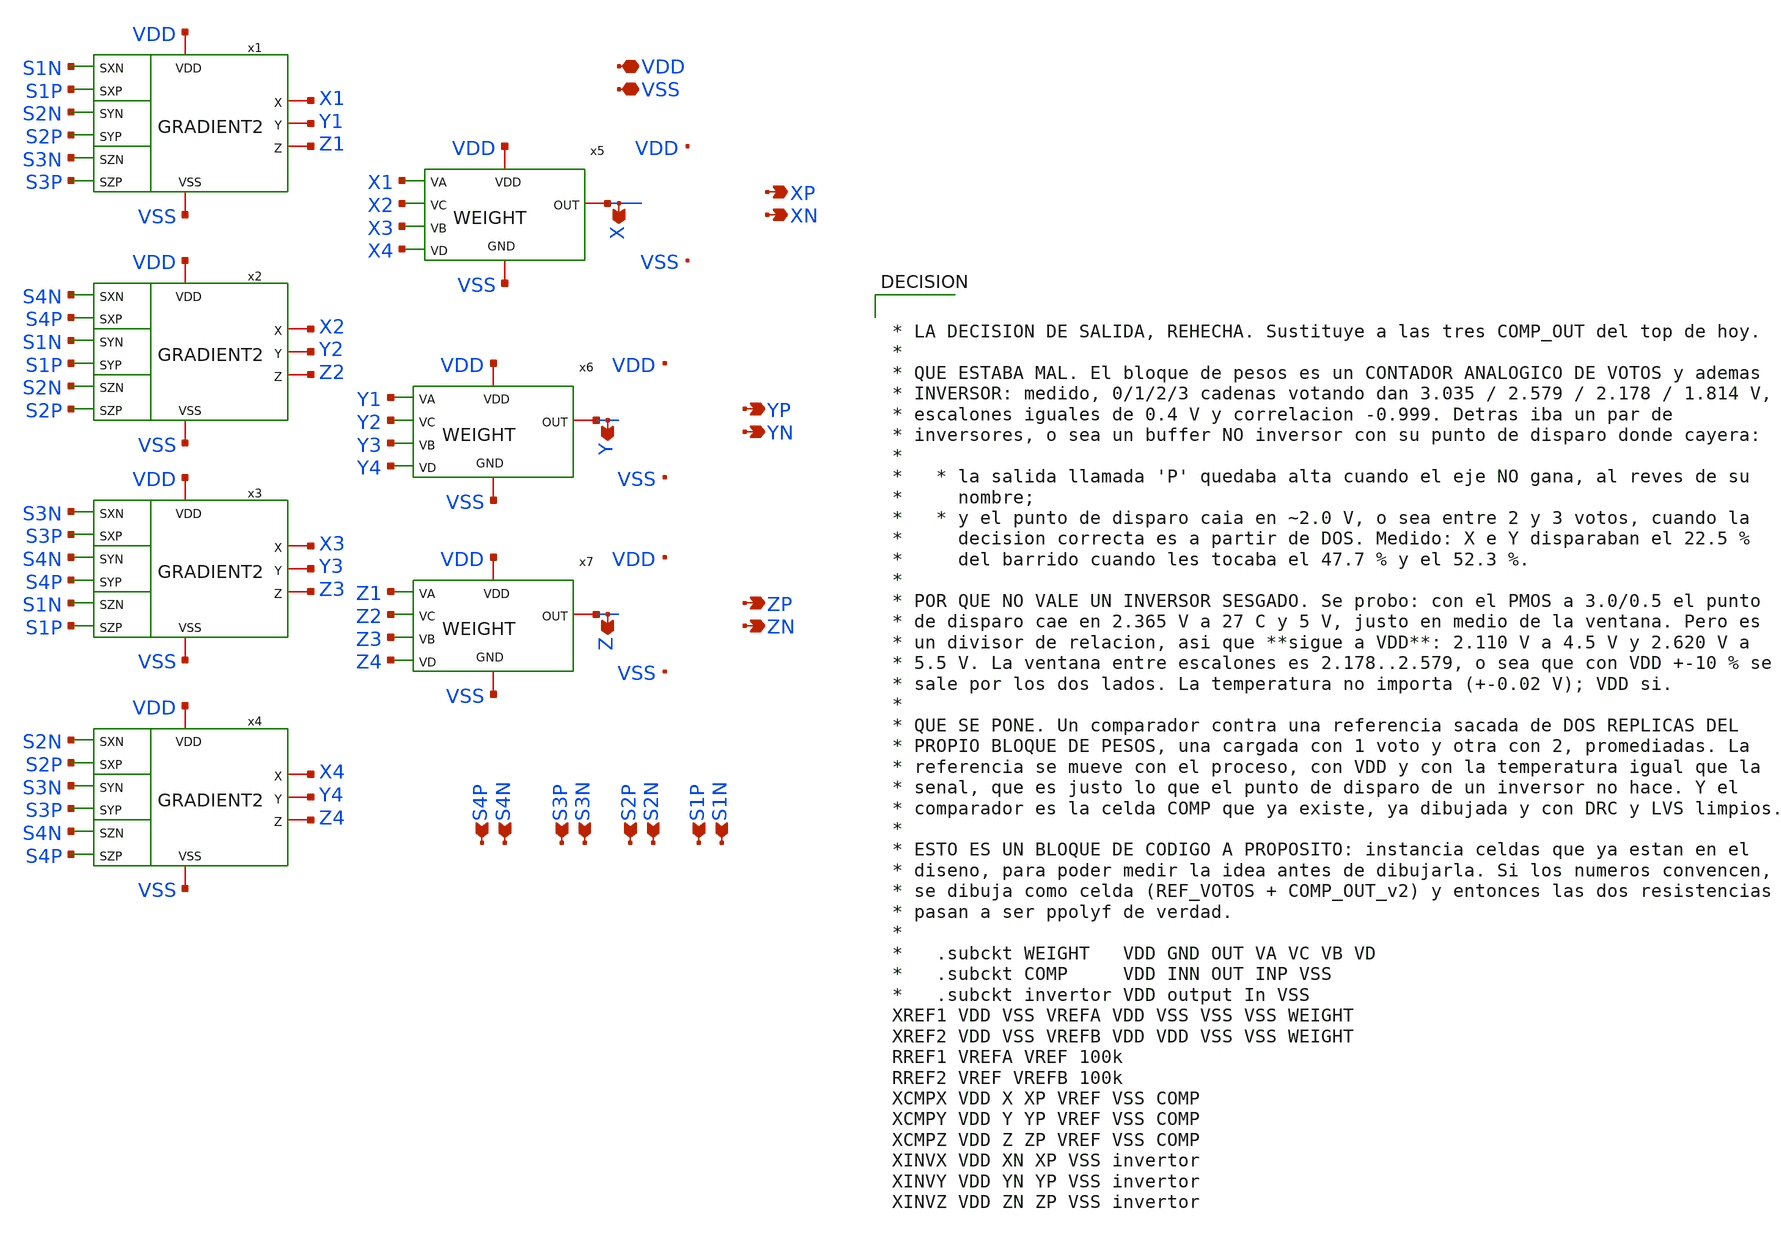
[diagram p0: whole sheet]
** sch_path: FINAL/XSCHEM_v2/GRADIENT_NAV2_V2.sch
**.subckt GRADIENT_NAV2_V2 S1N VDD XN VSS S1P S2N S2P S3N S3P S4N S4P XP YN YP ZN ZP X Y Z
*.ipin S1N
*.iopin VDD
*.opin XN
*.iopin VSS
*.ipin S1P
*.ipin S2N
*.ipin S2P
*.ipin S3N
*.ipin S3P
*.ipin S4N
*.ipin S4P
*.opin XP
*.opin YN
*.opin YP
*.opin ZN
*.opin ZP
*.opin X
*.opin Y
*.opin Z
x5 VDD VSS X X1 X2 X3 X4 WEIGHT
x6 VDD VSS Y Y1 Y2 Y3 Y4 WEIGHT
x7 VDD VSS Z Z1 Z2 Z3 Z4 WEIGHT
x1 S1N S1P VDD X1 S2N Y1 Z1 S2P VSS S3N S3P GRADIENT2
x2 S4N S4P VDD X2 S1N Y2 Z2 S1P VSS S2N S2P GRADIENT2
x3 S3N S3P VDD X3 S4N Y3 Z3 S4P VSS S1N S1P GRADIENT2
x4 S2N S2P VDD X4 S3N Y4 Z4 S3P VSS S4N S4P GRADIENT2
**** begin user architecture code


* Condensadores de desacople: NMOS y PMOS en inversion metidos en
* los huecos entre macros. LO ESCRIBE scripts/decap_fill.py -- no
* se edita a mano: tiene que ser exactamente lo que hay en el GDS.
XMdecn0 VSS VDD VSS VSS nfet_06v0 L=2.0u W=1.5u nf=1 m=1
XMdecn1 VSS VDD VSS VSS nfet_06v0 L=2.0u W=1.5u nf=1 m=1
XMdecn2 VSS VDD VSS VSS nfet_06v0 L=2.0u W=1.5u nf=1 m=1
XMdecn3 VSS VDD VSS VSS nfet_06v0 L=2.0u W=1.5u nf=1 m=1
XMdecn4 VSS VDD VSS VSS nfet_06v0 L=2.0u W=1.5u nf=1 m=1
XMdecn5 VSS VDD VSS VSS nfet_06v0 L=2.0u W=1.5u nf=1 m=1
XMdecn6 VSS VDD VSS VSS nfet_06v0 L=2.0u W=1.5u nf=1 m=1
XMdecn7 VSS VDD VSS VSS nfet_06v0 L=2.0u W=1.5u nf=1 m=1
XMdecn8 VSS VDD VSS VSS nfet_06v0 L=2.0u W=1.5u nf=1 m=1
XMdecn9 VSS VDD VSS VSS nfet_06v0 L=2.0u W=1.5u nf=1 m=1
XMdecn10 VSS VDD VSS VSS nfet_06v0 L=2.0u W=1.5u nf=1 m=1
XMdecn11 VSS VDD VSS VSS nfet_06v0 L=2.0u W=1.5u nf=1 m=1
XMdecn12 VSS VDD VSS VSS nfet_06v0 L=2.0u W=1.5u nf=1 m=1
XMdecn13 VSS VDD VSS VSS nfet_06v0 L=2.0u W=1.5u nf=1 m=1
XMdecn14 VSS VDD VSS VSS nfet_06v0 L=2.0u W=1.5u nf=1 m=1
XMdecn15 VSS VDD VSS VSS nfet_06v0 L=2.0u W=1.5u nf=1 m=1
XMdecn16 VSS VDD VSS VSS nfet_06v0 L=2.0u W=1.5u nf=1 m=1
XMdecn17 VSS VDD VSS VSS nfet_06v0 L=2.0u W=1.5u nf=1 m=1
XMdecn18 VSS VDD VSS VSS nfet_06v0 L=2.0u W=1.5u nf=1 m=1
XMdecn19 VSS VDD VSS VSS nfet_06v0 L=2.0u W=1.5u nf=1 m=1
XMdecn20 VSS VDD VSS VSS nfet_06v0 L=2.0u W=1.5u nf=1 m=1
XMdecn21 VSS VDD VSS VSS nfet_06v0 L=2.0u W=1.5u nf=1 m=1
XMdecn22 VSS VDD VSS VSS nfet_06v0 L=2.0u W=1.5u nf=1 m=1
XMdecn23 VSS VDD VSS VSS nfet_06v0 L=2.0u W=1.5u nf=1 m=1
XMdecn24 VSS VDD VSS VSS nfet_06v0 L=2.0u W=1.5u nf=1 m=1
XMdecn25 VSS VDD VSS VSS nfet_06v0 L=2.0u W=1.5u nf=1 m=1
XMdecn26 VSS VDD VSS VSS nfet_06v0 L=2.0u W=1.5u nf=1 m=1
XMdecn27 VSS VDD VSS VSS nfet_06v0 L=2.0u W=1.5u nf=1 m=1
XMdecn28 VSS VDD VSS VSS nfet_06v0 L=2.0u W=1.5u nf=1 m=1
XMdecn29 VSS VDD VSS VSS nfet_06v0 L=2.0u W=1.5u nf=1 m=1
XMdecn30 VSS VDD VSS VSS nfet_06v0 L=2.0u W=1.5u nf=1 m=1
XMdecn31 VSS VDD VSS VSS nfet_06v0 L=2.0u W=1.5u nf=1 m=1
XMdecn32 VSS VDD VSS VSS nfet_06v0 L=2.0u W=1.5u nf=1 m=1
XMdecn33 VSS VDD VSS VSS nfet_06v0 L=2.0u W=1.5u nf=1 m=1
XMdecn34 VSS VDD VSS VSS nfet_06v0 L=2.0u W=1.5u nf=1 m=1
XMdecn35 VSS VDD VSS VSS nfet_06v0 L=2.0u W=1.5u nf=1 m=1
XMdecn36 VSS VDD VSS VSS nfet_06v0 L=2.0u W=1.5u nf=1 m=1
XMdecn37 VSS VDD VSS VSS nfet_06v0 L=2.0u W=1.5u nf=1 m=1
XMdecn38 VSS VDD VSS VSS nfet_06v0 L=2.0u W=1.5u nf=1 m=1
XMdecn39 VSS VDD VSS VSS nfet_06v0 L=2.0u W=1.5u nf=1 m=1
XMdecn40 VSS VDD VSS VSS nfet_06v0 L=2.0u W=1.5u nf=1 m=1
XMdecn41 VSS VDD VSS VSS nfet_06v0 L=2.0u W=1.5u nf=1 m=1
XMdecn42 VSS VDD VSS VSS nfet_06v0 L=2.0u W=1.5u nf=1 m=1
XMdecn43 VSS VDD VSS VSS nfet_06v0 L=2.0u W=1.5u nf=1 m=1
XMdecn44 VSS VDD VSS VSS nfet_06v0 L=2.0u W=1.5u nf=1 m=1
XMdecn45 VSS VDD VSS VSS nfet_06v0 L=2.0u W=1.5u nf=1 m=1
XMdecn46 VSS VDD VSS VSS nfet_06v0 L=2.0u W=1.5u nf=1 m=1
XMdecn47 VSS VDD VSS VSS nfet_06v0 L=2.0u W=1.5u nf=1 m=1
XMdecn48 VSS VDD VSS VSS nfet_06v0 L=2.0u W=1.5u nf=1 m=1
XMdecn49 VSS VDD VSS VSS nfet_06v0 L=2.0u W=1.5u nf=1 m=1
XMdecn50 VSS VDD VSS VSS nfet_06v0 L=2.0u W=1.5u nf=1 m=1
XMdecn51 VSS VDD VSS VSS nfet_06v0 L=2.0u W=1.5u nf=1 m=1
XMdecn52 VSS VDD VSS VSS nfet_06v0 L=2.0u W=1.5u nf=1 m=1
XMdecp53 VDD VSS VDD VDD pfet_06v0 L=2.0u W=1.5u nf=1 m=1
XMdecp54 VDD VSS VDD VDD pfet_06v0 L=2.0u W=1.5u nf=1 m=1
XMdecp55 VDD VSS VDD VDD pfet_06v0 L=2.0u W=1.5u nf=1 m=1
XMdecp56 VDD VSS VDD VDD pfet_06v0 L=2.0u W=1.5u nf=1 m=1
XMdecp57 VDD VSS VDD VDD pfet_06v0 L=2.0u W=1.5u nf=1 m=1
XMdecp58 VDD VSS VDD VDD pfet_06v0 L=2.0u W=1.5u nf=1 m=1
XMdecp59 VDD VSS VDD VDD pfet_06v0 L=2.0u W=1.5u nf=1 m=1
XMdecp60 VDD VSS VDD VDD pfet_06v0 L=2.0u W=1.5u nf=1 m=1
XMdecp61 VDD VSS VDD VDD pfet_06v0 L=2.0u W=1.5u nf=1 m=1
XMdecp62 VDD VSS VDD VDD pfet_06v0 L=2.0u W=1.5u nf=1 m=1
XMdecp63 VDD VSS VDD VDD pfet_06v0 L=2.0u W=1.5u nf=1 m=1
XMdecp64 VDD VSS VDD VDD pfet_06v0 L=2.0u W=1.5u nf=1 m=1
XMdecp65 VDD VSS VDD VDD pfet_06v0 L=2.0u W=1.5u nf=1 m=1
XMdecp66 VDD VSS VDD VDD pfet_06v0 L=2.0u W=1.5u nf=1 m=1
XMdecp67 VDD VSS VDD VDD pfet_06v0 L=2.0u W=1.5u nf=1 m=1
XMdecp68 VDD VSS VDD VDD pfet_06v0 L=2.0u W=1.5u nf=1 m=1
XMdecp69 VDD VSS VDD VDD pfet_06v0 L=2.0u W=1.5u nf=1 m=1
XMdecp70 VDD VSS VDD VDD pfet_06v0 L=2.0u W=1.5u nf=1 m=1
XMdecp71 VDD VSS VDD VDD pfet_06v0 L=2.0u W=1.5u nf=1 m=1
XMdecp72 VDD VSS VDD VDD pfet_06v0 L=2.0u W=1.5u nf=1 m=1
XMdecp73 VDD VSS VDD VDD pfet_06v0 L=2.0u W=1.5u nf=1 m=1
XMdecp74 VDD VSS VDD VDD pfet_06v0 L=2.0u W=1.5u nf=1 m=1
XMdecp75 VDD VSS VDD VDD pfet_06v0 L=2.0u W=1.5u nf=1 m=1
XMdecp76 VDD VSS VDD VDD pfet_06v0 L=2.0u W=1.5u nf=1 m=1
XMdecp77 VDD VSS VDD VDD pfet_06v0 L=2.0u W=1.5u nf=1 m=1
XMdecp78 VDD VSS VDD VDD pfet_06v0 L=2.0u W=1.5u nf=1 m=1
XMdecp79 VDD VSS VDD VDD pfet_06v0 L=2.0u W=1.5u nf=1 m=1
XMdecp80 VDD VSS VDD VDD pfet_06v0 L=2.0u W=1.5u nf=1 m=1
XMdecp81 VDD VSS VDD VDD pfet_06v0 L=2.0u W=1.5u nf=1 m=1
XMdecp82 VDD VSS VDD VDD pfet_06v0 L=2.0u W=1.5u nf=1 m=1
XMdecp83 VDD VSS VDD VDD pfet_06v0 L=2.0u W=1.5u nf=1 m=1
XMdecp84 VDD VSS VDD VDD pfet_06v0 L=2.0u W=1.5u nf=1 m=1
XMdecp85 VDD VSS VDD VDD pfet_06v0 L=2.0u W=1.5u nf=1 m=1
XMdecp86 VDD VSS VDD VDD pfet_06v0 L=2.0u W=1.5u nf=1 m=1
XMdecp87 VDD VSS VDD VDD pfet_06v0 L=2.0u W=1.5u nf=1 m=1
XMdecp88 VDD VSS VDD VDD pfet_06v0 L=2.0u W=1.5u nf=1 m=1
XMdecp89 VDD VSS VDD VDD pfet_06v0 L=2.0u W=1.5u nf=1 m=1
XMdecp90 VDD VSS VDD VDD pfet_06v0 L=2.0u W=1.5u nf=1 m=1
XMdecp91 VDD VSS VDD VDD pfet_06v0 L=2.0u W=1.5u nf=1 m=1
XMdecp92 VDD VSS VDD VDD pfet_06v0 L=2.0u W=1.5u nf=1 m=1
XMdecp93 VDD VSS VDD VDD pfet_06v0 L=2.0u W=1.5u nf=1 m=1
XMdecp94 VDD VSS VDD VDD pfet_06v0 L=2.0u W=1.5u nf=1 m=1
XMdecp95 VDD VSS VDD VDD pfet_06v0 L=2.0u W=1.5u nf=1 m=1
XMdecp96 VDD VSS VDD VDD pfet_06v0 L=2.0u W=1.5u nf=1 m=1
XMdecp97 VDD VSS VDD VDD pfet_06v0 L=2.0u W=1.5u nf=1 m=1
XMdecp98 VDD VSS VDD VDD pfet_06v0 L=2.0u W=1.5u nf=1 m=1
XMdecp99 VDD VSS VDD VDD pfet_06v0 L=2.0u W=1.5u nf=1 m=1
XMdecp100 VDD VSS VDD VDD pfet_06v0 L=2.0u W=1.5u nf=1 m=1
XMdecp101 VDD VSS VDD VDD pfet_06v0 L=2.0u W=1.5u nf=1 m=1
XMdecn102 VSS VDD VSS VSS nfet_06v0 L=2.0u W=18.0u nf=1 m=1
XMdecn103 VSS VDD VSS VSS nfet_06v0 L=2.0u W=18.0u nf=1 m=1
XMdecp104 VDD VSS VDD VDD pfet_06v0 L=2.0u W=18.0u nf=1 m=1
XMdecp105 VDD VSS VDD VDD pfet_06v0 L=2.0u W=18.0u nf=1 m=1
XMdecn106 VSS VDD VSS VSS nfet_06v0 L=2.0u W=18.0u nf=1 m=1
XMdecn107 VSS VDD VSS VSS nfet_06v0 L=2.0u W=18.0u nf=1 m=1
XMdecp108 VDD VSS VDD VDD pfet_06v0 L=2.0u W=18.0u nf=1 m=1
XMdecp109 VDD VSS VDD VDD pfet_06v0 L=2.0u W=18.0u nf=1 m=1
XMdecn110 VSS VDD VSS VSS nfet_06v0 L=2.0u W=18.0u nf=1 m=1
XMdecn111 VSS VDD VSS VSS nfet_06v0 L=2.0u W=18.0u nf=1 m=1
XMdecp112 VDD VSS VDD VDD pfet_06v0 L=2.0u W=18.0u nf=1 m=1
XMdecp113 VDD VSS VDD VDD pfet_06v0 L=2.0u W=18.0u nf=1 m=1
XMdecn114 VSS VDD VSS VSS nfet_06v0 L=2.0u W=18.0u nf=1 m=1
XMdecn115 VSS VDD VSS VSS nfet_06v0 L=2.0u W=18.0u nf=1 m=1
XMdecp116 VDD VSS VDD VDD pfet_06v0 L=2.0u W=18.0u nf=1 m=1
XMdecp117 VDD VSS VDD VDD pfet_06v0 L=2.0u W=18.0u nf=1 m=1
XMdecn118 VSS VDD VSS VSS nfet_06v0 L=2.0u W=18.0u nf=1 m=1
XMdecn119 VSS VDD VSS VSS nfet_06v0 L=2.0u W=18.0u nf=1 m=1
XMdecp120 VDD VSS VDD VDD pfet_06v0 L=2.0u W=18.0u nf=1 m=1
XMdecp121 VDD VSS VDD VDD pfet_06v0 L=2.0u W=18.0u nf=1 m=1
XMdecn122 VSS VDD VSS VSS nfet_06v0 L=2.0u W=18.0u nf=1 m=1
XMdecn123 VSS VDD VSS VSS nfet_06v0 L=2.0u W=18.0u nf=1 m=1
XMdecp124 VDD VSS VDD VDD pfet_06v0 L=2.0u W=18.0u nf=1 m=1
XMdecp125 VDD VSS VDD VDD pfet_06v0 L=2.0u W=18.0u nf=1 m=1
XMdecn126 VSS VDD VSS VSS nfet_06v0 L=2.0u W=18.0u nf=1 m=1
XMdecn127 VSS VDD VSS VSS nfet_06v0 L=2.0u W=18.0u nf=1 m=1
XMdecp128 VDD VSS VDD VDD pfet_06v0 L=2.0u W=18.0u nf=1 m=1
XMdecp129 VDD VSS VDD VDD pfet_06v0 L=2.0u W=18.0u nf=1 m=1
XMdecn130 VSS VDD VSS VSS nfet_06v0 L=2.0u W=18.0u nf=1 m=1
XMdecn131 VSS VDD VSS VSS nfet_06v0 L=2.0u W=18.0u nf=1 m=1
XMdecp132 VDD VSS VDD VDD pfet_06v0 L=2.0u W=18.0u nf=1 m=1
XMdecp133 VDD VSS VDD VDD pfet_06v0 L=2.0u W=18.0u nf=1 m=1
XMdecn134 VSS VDD VSS VSS nfet_06v0 L=2.0u W=18.0u nf=1 m=1
XMdecn135 VSS VDD VSS VSS nfet_06v0 L=2.0u W=18.0u nf=1 m=1
XMdecp136 VDD VSS VDD VDD pfet_06v0 L=2.0u W=18.0u nf=1 m=1
XMdecp137 VDD VSS VDD VDD pfet_06v0 L=2.0u W=18.0u nf=1 m=1
XMdecn138 VSS VDD VSS VSS nfet_06v0 L=2.0u W=18.0u nf=1 m=1
XMdecp139 VDD VSS VDD VDD pfet_06v0 L=2.0u W=18.0u nf=1 m=1
XMdecn140 VSS VDD VSS VSS nfet_06v0 L=2.0u W=18.0u nf=1 m=1
XMdecp141 VDD VSS VDD VDD pfet_06v0 L=2.0u W=18.0u nf=1 m=1
XMdecn142 VSS VDD VSS VSS nfet_06v0 L=2.0u W=18.0u nf=1 m=1
XMdecp143 VDD VSS VDD VDD pfet_06v0 L=2.0u W=18.0u nf=1 m=1
XMdecn144 VSS VDD VSS VSS nfet_06v0 L=2.0u W=9.75u nf=1 m=1
XMdecn145 VSS VDD VSS VSS nfet_06v0 L=2.0u W=9.75u nf=1 m=1
XMdecp146 VDD VSS VDD VDD pfet_06v0 L=2.0u W=9.75u nf=1 m=1
XMdecp147 VDD VSS VDD VDD pfet_06v0 L=2.0u W=9.75u nf=1 m=1
XMdecn148 VSS VDD VSS VSS nfet_06v0 L=2.0u W=9.75u nf=1 m=1
XMdecn149 VSS VDD VSS VSS nfet_06v0 L=2.0u W=9.75u nf=1 m=1
XMdecp150 VDD VSS VDD VDD pfet_06v0 L=2.0u W=9.75u nf=1 m=1
XMdecp151 VDD VSS VDD VDD pfet_06v0 L=2.0u W=9.75u nf=1 m=1
XMdecn152 VSS VDD VSS VSS nfet_06v0 L=2.0u W=9.75u nf=1 m=1
XMdecn153 VSS VDD VSS VSS nfet_06v0 L=2.0u W=9.75u nf=1 m=1
XMdecp154 VDD VSS VDD VDD pfet_06v0 L=2.0u W=9.75u nf=1 m=1
XMdecp155 VDD VSS VDD VDD pfet_06v0 L=2.0u W=9.75u nf=1 m=1
XMdecn156 VSS VDD VSS VSS nfet_06v0 L=2.0u W=9.75u nf=1 m=1
XMdecn157 VSS VDD VSS VSS nfet_06v0 L=2.0u W=9.75u nf=1 m=1
XMdecp158 VDD VSS VDD VDD pfet_06v0 L=2.0u W=9.75u nf=1 m=1
XMdecp159 VDD VSS VDD VDD pfet_06v0 L=2.0u W=9.75u nf=1 m=1
XMdecn160 VSS VDD VSS VSS nfet_06v0 L=2.0u W=9.75u nf=1 m=1
XMdecn161 VSS VDD VSS VSS nfet_06v0 L=2.0u W=9.75u nf=1 m=1
XMdecp162 VDD VSS VDD VDD pfet_06v0 L=2.0u W=9.75u nf=1 m=1
XMdecp163 VDD VSS VDD VDD pfet_06v0 L=2.0u W=9.75u nf=1 m=1
XMdecn164 VSS VDD VSS VSS nfet_06v0 L=2.0u W=9.75u nf=1 m=1
XMdecn165 VSS VDD VSS VSS nfet_06v0 L=2.0u W=9.75u nf=1 m=1
XMdecp166 VDD VSS VDD VDD pfet_06v0 L=2.0u W=9.75u nf=1 m=1
XMdecp167 VDD VSS VDD VDD pfet_06v0 L=2.0u W=9.75u nf=1 m=1
XMdecn168 VSS VDD VSS VSS nfet_06v0 L=2.0u W=9.75u nf=1 m=1
XMdecn169 VSS VDD VSS VSS nfet_06v0 L=2.0u W=9.75u nf=1 m=1
XMdecp170 VDD VSS VDD VDD pfet_06v0 L=2.0u W=9.75u nf=1 m=1
XMdecp171 VDD VSS VDD VDD pfet_06v0 L=2.0u W=9.75u nf=1 m=1
XMdecn172 VSS VDD VSS VSS nfet_06v0 L=2.0u W=9.75u nf=1 m=1
XMdecn173 VSS VDD VSS VSS nfet_06v0 L=2.0u W=9.75u nf=1 m=1
XMdecp174 VDD VSS VDD VDD pfet_06v0 L=2.0u W=9.75u nf=1 m=1
XMdecp175 VDD VSS VDD VDD pfet_06v0 L=2.0u W=9.75u nf=1 m=1
XMdecn176 VSS VDD VSS VSS nfet_06v0 L=2.0u W=9.75u nf=1 m=1
XMdecn177 VSS VDD VSS VSS nfet_06v0 L=2.0u W=9.75u nf=1 m=1
XMdecp178 VDD VSS VDD VDD pfet_06v0 L=2.0u W=9.75u nf=1 m=1
XMdecp179 VDD VSS VDD VDD pfet_06v0 L=2.0u W=9.75u nf=1 m=1
XMdecn180 VSS VDD VSS VSS nfet_06v0 L=2.0u W=9.75u nf=1 m=1
XMdecn181 VSS VDD VSS VSS nfet_06v0 L=2.0u W=9.75u nf=1 m=1
XMdecp182 VDD VSS VDD VDD pfet_06v0 L=2.0u W=9.75u nf=1 m=1
XMdecp183 VDD VSS VDD VDD pfet_06v0 L=2.0u W=9.75u nf=1 m=1
XMdecn184 VSS VDD VSS VSS nfet_06v0 L=2.0u W=9.75u nf=1 m=1
XMdecn185 VSS VDD VSS VSS nfet_06v0 L=2.0u W=9.75u nf=1 m=1
XMdecp186 VDD VSS VDD VDD pfet_06v0 L=2.0u W=9.75u nf=1 m=1
XMdecp187 VDD VSS VDD VDD pfet_06v0 L=2.0u W=9.75u nf=1 m=1
XMdecn188 VSS VDD VSS VSS nfet_06v0 L=2.0u W=9.75u nf=1 m=1
XMdecn189 VSS VDD VSS VSS nfet_06v0 L=2.0u W=9.75u nf=1 m=1
XMdecp190 VDD VSS VDD VDD pfet_06v0 L=2.0u W=9.75u nf=1 m=1
XMdecp191 VDD VSS VDD VDD pfet_06v0 L=2.0u W=9.75u nf=1 m=1
XMdecn192 VSS VDD VSS VSS nfet_06v0 L=2.0u W=18.0u nf=1 m=1
XMdecp193 VDD VSS VDD VDD pfet_06v0 L=2.0u W=18.0u nf=1 m=1
XMdecn194 VSS VDD VSS VSS nfet_06v0 L=2.0u W=18.0u nf=1 m=1
XMdecp195 VDD VSS VDD VDD pfet_06v0 L=2.0u W=18.0u nf=1 m=1
XMdecn196 VSS VDD VSS VSS nfet_06v0 L=2.0u W=18.0u nf=1 m=1
XMdecp197 VDD VSS VDD VDD pfet_06v0 L=2.0u W=18.0u nf=1 m=1
XMdecn198 VSS VDD VSS VSS nfet_06v0 L=2.0u W=1.5u nf=1 m=1
XMdecn199 VSS VDD VSS VSS nfet_06v0 L=2.0u W=1.5u nf=1 m=1
XMdecn200 VSS VDD VSS VSS nfet_06v0 L=2.0u W=1.5u nf=1 m=1
XMdecn201 VSS VDD VSS VSS nfet_06v0 L=2.0u W=1.5u nf=1 m=1
XMdecp202 VDD VSS VDD VDD pfet_06v0 L=2.0u W=1.5u nf=1 m=1
XMdecp203 VDD VSS VDD VDD pfet_06v0 L=2.0u W=1.5u nf=1 m=1
XMdecp204 VDD VSS VDD VDD pfet_06v0 L=2.0u W=1.5u nf=1 m=1
XMdecp205 VDD VSS VDD VDD pfet_06v0 L=2.0u W=1.5u nf=1 m=1
XMdecn206 VSS VDD VSS VSS nfet_06v0 L=2.0u W=9.75u nf=1 m=1
XMdecp207 VDD VSS VDD VDD pfet_06v0 L=2.0u W=9.75u nf=1 m=1
XMdecn208 VSS VDD VSS VSS nfet_06v0 L=2.0u W=9.75u nf=1 m=1
XMdecp209 VDD VSS VDD VDD pfet_06v0 L=2.0u W=9.75u nf=1 m=1
XMdecn210 VSS VDD VSS VSS nfet_06v0 L=2.0u W=9.75u nf=1 m=1
XMdecp211 VDD VSS VDD VDD pfet_06v0 L=2.0u W=9.75u nf=1 m=1
XMdecn212 VSS VDD VSS VSS nfet_06v0 L=2.0u W=9.75u nf=1 m=1
XMdecp213 VDD VSS VDD VDD pfet_06v0 L=2.0u W=9.75u nf=1 m=1
XMdecn214 VSS VDD VSS VSS nfet_06v0 L=2.0u W=1.5u nf=1 m=1
XMdecn215 VSS VDD VSS VSS nfet_06v0 L=2.0u W=1.5u nf=1 m=1
XMdecp216 VDD VSS VDD VDD pfet_06v0 L=2.0u W=1.5u nf=1 m=1
XMdecp217 VDD VSS VDD VDD pfet_06v0 L=2.0u W=1.5u nf=1 m=1
XMdecn218 VSS VDD VSS VSS nfet_06v0 L=2.0u W=1.5u nf=1 m=1
XMdecn219 VSS VDD VSS VSS nfet_06v0 L=2.0u W=1.5u nf=1 m=1
XMdecp220 VDD VSS VDD VDD pfet_06v0 L=2.0u W=1.5u nf=1 m=1
XMdecp221 VDD VSS VDD VDD pfet_06v0 L=2.0u W=1.5u nf=1 m=1
XMdecn222 VSS VDD VSS VSS nfet_06v0 L=2.0u W=1.5u nf=1 m=1
XMdecp223 VDD VSS VDD VDD pfet_06v0 L=2.0u W=1.5u nf=1 m=1




* LA DECISION DE SALIDA, REHECHA. Sustituye a las tres COMP_OUT del top de hoy.
*
* QUE ESTABA MAL. El bloque de pesos es un CONTADOR ANALOGICO DE VOTOS y ademas
* INVERSOR: medido, 0/1/2/3 cadenas votando dan 3.035 / 2.579 / 2.178 / 1.814 V,
* escalones iguales de 0.4 V y correlacion -0.999. Detras iba un par de
* inversores, o sea un buffer NO inversor con su punto de disparo donde cayera:
*
*   * la salida llamada 'P' quedaba alta cuando el eje NO gana, al reves de su
*     nombre;
*   * y el punto de disparo caia en ~2.0 V, o sea entre 2 y 3 votos, cuando la
*     decision correcta es a partir de DOS. Medido: X e Y disparaban el 22.5 %
*     del barrido cuando les tocaba el 47.7 % y el 52.3 %.
*
* POR QUE NO VALE UN INVERSOR SESGADO. Se probo: con el PMOS a 3.0/0.5 el punto
* de disparo cae en 2.365 V a 27 C y 5 V, justo en medio de la ventana. Pero es
* un divisor de relacion, asi que **sigue a VDD**: 2.110 V a 4.5 V y 2.620 V a
* 5.5 V. La ventana entre escalones es 2.178..2.579, o sea que con VDD +-10 % se
* sale por los dos lados. La temperatura no importa (+-0.02 V); VDD si.
*
* QUE SE PONE. Un comparador contra una referencia sacada de DOS REPLICAS DEL
* PROPIO BLOQUE DE PESOS, una cargada con 1 voto y otra con 2, promediadas. La
* referencia se mueve con el proceso, con VDD y con la temperatura igual que la
* senal, que es justo lo que el punto de disparo de un inversor no hace. Y el
* comparador es la celda COMP que ya existe, ya dibujada y con DRC y LVS limpios.
*
* ESTO ES UN BLOQUE DE CODIGO A PROPOSITO: instancia celdas que ya estan en el
* diseno, para poder medir la idea antes de dibujarla. Si los numeros convencen,
* se dibuja como celda (REF_VOTOS + COMP_OUT_v2) y entonces las dos resistencias
* pasan a ser ppolyf de verdad.
*
*   .subckt WEIGHT   VDD GND OUT VA VC VB VD
*   .subckt COMP     VDD INN OUT INP VSS
*   .subckt invertor VDD output In VSS
XREF1 VDD VSS VREFA VDD VSS VSS VSS WEIGHT
XREF2 VDD VSS VREFB VDD VDD VSS VSS WEIGHT
RREF1 VREFA VREF 100k
RREF2 VREF VREFB 100k
XCMPX VDD X XP VREF VSS COMP
XCMPY VDD Y YP VREF VSS COMP
XCMPZ VDD Z ZP VREF VSS COMP
XINVX VDD XN XP VSS invertor
XINVY VDD YN YP VSS invertor
XINVZ VDD ZN ZP VSS invertor


**** end user architecture code
**.ends
.end
